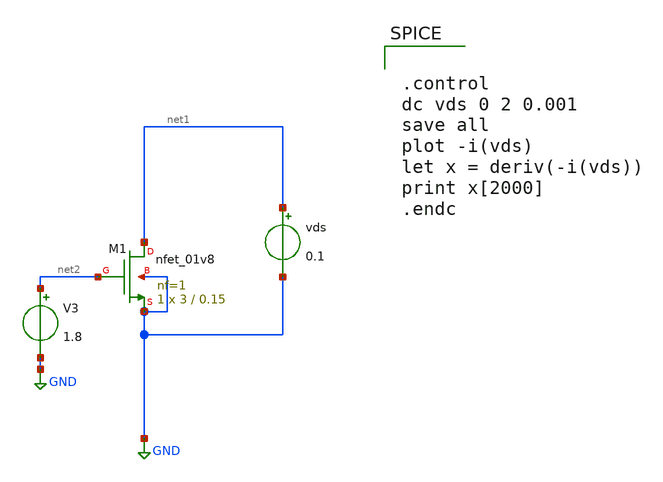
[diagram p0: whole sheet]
** sch_path: mos_sizing/moschar_deeptriode.sch
**.subckt moschar_deeptriode
XM1 net1 net2 GND GND sky130_fd_pr__nfet_01v8 L=0.15 W=3 nf=1 ad='int((nf+1)/2) * W/nf * 0.29' as='int((nf+2)/2) * W/nf * 0.29'
+ pd='2*int((nf+1)/2) * (W/nf + 0.29)' ps='2*int((nf+2)/2) * (W/nf + 0.29)' nrd='0.29 / W' nrs='0.29 / W'
+ sa=0 sb=0 sd=0 mult=1 m=1
vds net1 GND 0.1
V3 net2 GND 1.8
**** begin user architecture code


.option wnflag = 1
.lib /usr/local/share/pdk/sky130A/libs.tech/ngspice/sky130.lib.spice tt
.include /usr/local/share/pdk/sky130A/libs.ref/sky130_fd_pr/spice/sky130_fd_pr__ind_05_220.model.spice
.param mc_mm_switch=0




.control
dc vds 0 2 0.001
save all
plot -i(vds)
let x = deriv(-i(vds))
print x[2000]
.endc


**** end user architecture code
**.ends
.GLOBAL GND
.end
